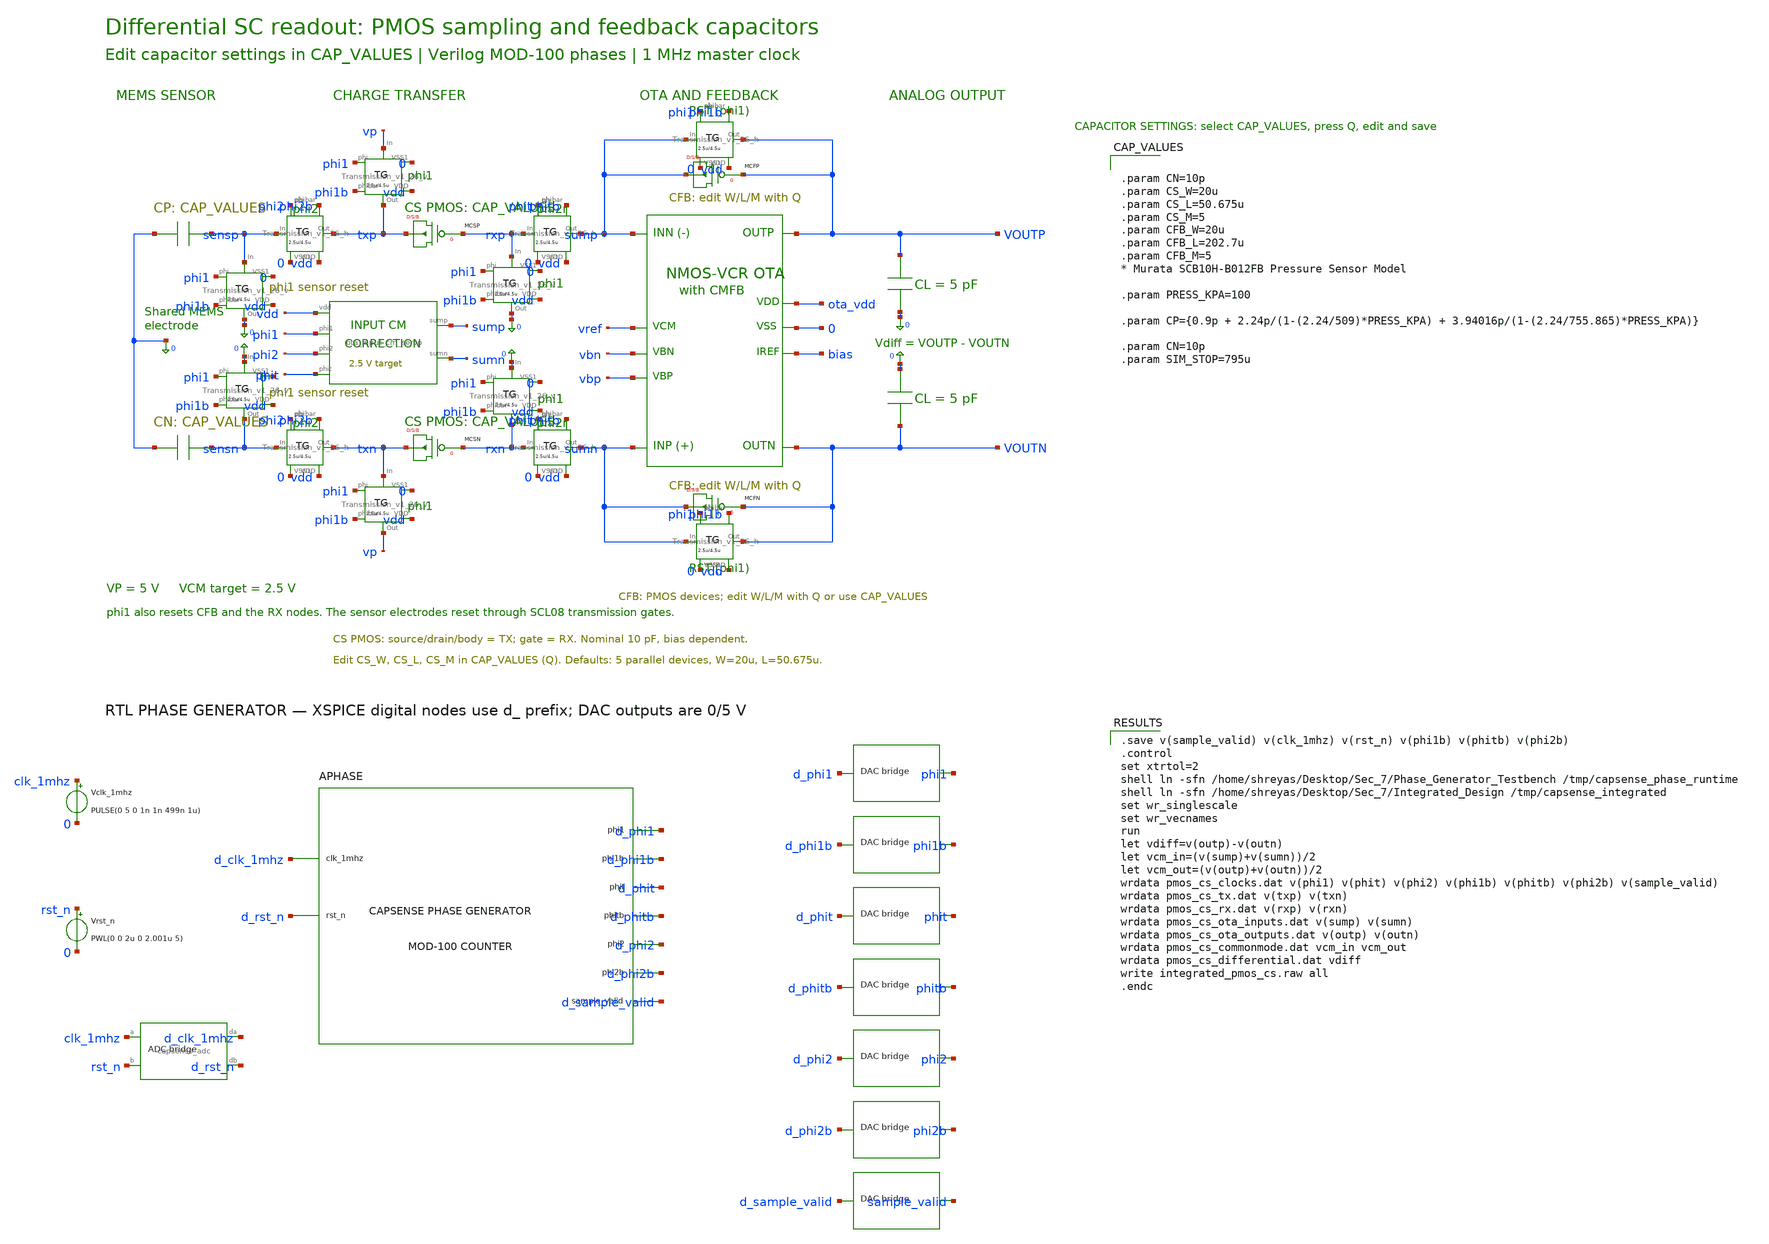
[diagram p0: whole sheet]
** sch_path: Mixed_Signal/Integrated_Design/schematic/capsense_integrated_pmos_cs_tb.sch
**.subckt capsense_integrated_pmos_cs_tb
XOTA sumn sump outp outn ota_vdd 0 bias vref vbn vbp ota_telescopic_cm2p5
CMEMP 0 sensp {CP}
XSENSEP phi2 0 sensp txp vdd phi2b Transmission_v1_26_h
XSRESETP phi1 0 sensp 0 vdd phi1b Transmission_v1_26_v
XCHARGEP phi1 0 vp txp vdd phi1b Transmission_v1_26_v
MCSP txp rxp txp txp P W={CS_W} L={CS_L} M={CS_M} AD='( {CS_W} ) * 4.5u' AS='( {CS_W} ) * 4.5u' PD='2 * ( {CS_W} ) + 9u'
+ PS='2 * ( {CS_W} ) + 9u'
XRRESETP phi1 0 rxp 0 vdd phi1b Transmission_v1_26_v
XXFERP phit 0 rxp sump vdd phitb Transmission_v1_26_h
MCFP sump outp sump sump P W={CFB_W} L={CFB_L} M={CFB_M} AD='( {CFB_W} ) * 4.5u' AS='( {CFB_W} ) * 4.5u'
+ PD='2 * ( {CFB_W} ) + 9u' PS='2 * ( {CFB_W} ) + 9u'
XFBRESETP phi1 0 sump outp vdd phi1b Transmission_v1_26_h
CLP outp 0 5p
CMEMN 0 sensn {CN}
XSENSEN phi2 0 sensn txn vdd phi2b Transmission_v1_26_h
XSRESETN phi1 0 0 sensn vdd phi1b Transmission_v1_26_v
XCHARGEN phi1 0 txn vp vdd phi1b Transmission_v1_26_v
MCSN txn rxn txn txn P W={CS_W} L={CS_L} M={CS_M} AD='( {CS_W} ) * 4.5u' AS='( {CS_W} ) * 4.5u' PD='2 * ( {CS_W} ) + 9u'
+ PS='2 * ( {CS_W} ) + 9u'
XRRESETN phi1 0 0 rxn vdd phi1b Transmission_v1_26_v
XXFERN phit 0 rxn sumn vdd phitb Transmission_v1_26_h
MCFN sumn outn sumn sumn P W={CFB_W} L={CFB_L} M={CFB_M} AD='( {CFB_W} ) * 4.5u' AS='( {CFB_W} ) * 4.5u'
+ PD='2 * ( {CFB_W} ) + 9u' PS='2 * ( {CFB_W} ) + 9u'
XFBRESETN phi1 0 sumn outn vdd phi1b Transmission_v1_26_h
CLN 0 outn 5p
XICM sump sumn vdd phi1 phi2 phit ota_input_cm_servo
APHASE [ d_clk_1mhz d_rst_n ] [ d_phi1 d_phit d_phi2 d_phi1b d_phitb d_phi2b d_sample_valid ] null
+ capsense_phase_gen_cosim
Vclk_1mhz clk_1mhz 0 PULSE(0 5 0 1n 1n 499n 1u)
Vrst_n rst_n 0 PWL(0 0 2u 0 2.001u 5)
AINPUTS [ clk_1mhz rst_n ] [ d_clk_1mhz d_rst_n ] capsense_adc
ADAC_phi1 [ d_phi1 ] [ phi1 ] capsense_dac
ADAC_phi1b [ d_phi1b ] [ phi1b ] capsense_dac
ADAC_phit [ d_phit ] [ phit ] capsense_dac
ADAC_phitb [ d_phitb ] [ phitb ] capsense_dac
ADAC_phi2 [ d_phi2 ] [ phi2 ] capsense_dac
ADAC_phi2b [ d_phi2b ] [ phi2b ] capsense_dac
ADAC_sample_valid [ d_sample_valid ] [ sample_valid ] capsense_dac
**** begin user architecture code
.include /home/shreyas/Desktop/Sec_7/Integrated_Design/simulation/analog_support.spice
.include /home/shreyas/Desktop/Sec_7/Integrated_Design/simulation/cosim_models.spice

.save v(sample_valid) v(clk_1mhz) v(rst_n) v(phi1b) v(phitb) v(phi2b)
.control
set xtrtol=2
shell ln -sfn /home/shreyas/Desktop/Sec_7/Phase_Generator_Testbench /tmp/capsense_phase_runtime
shell ln -sfn /home/shreyas/Desktop/Sec_7/Integrated_Design /tmp/capsense_integrated
set wr_singlescale
set wr_vecnames
run
let vdiff=v(outp)-v(outn)
let vcm_in=(v(sump)+v(sumn))/2
let vcm_out=(v(outp)+v(outn))/2
wrdata pmos_cs_clocks.dat v(phi1) v(phit) v(phi2) v(phi1b) v(phitb) v(phi2b) v(sample_valid)
wrdata pmos_cs_tx.dat v(txp) v(txn)
wrdata pmos_cs_rx.dat v(rxp) v(rxn)
wrdata pmos_cs_ota_inputs.dat v(sump) v(sumn)
wrdata pmos_cs_ota_outputs.dat v(outp) v(outn)
wrdata pmos_cs_commonmode.dat vcm_in vcm_out
wrdata pmos_cs_differential.dat vdiff
write integrated_pmos_cs.raw all
.endc



.param CN=10p
.param CS_W=20u
.param CS_L=50.675u
.param CS_M=5
.param CFB_W=20u
.param CFB_L=202.7u
.param CFB_M=5
* Murata SCB10H-B012FB Pressure Sensor Model

.param PRESS_KPA=100

.param CP={0.9p + 2.24p/(1-(2.24/509)*PRESS_KPA) + 3.94016p/(1-(2.24/755.865)*PRESS_KPA)}

.param CN=10p
.param SIM_STOP=795u

**** end user architecture code
**.ends
.end
